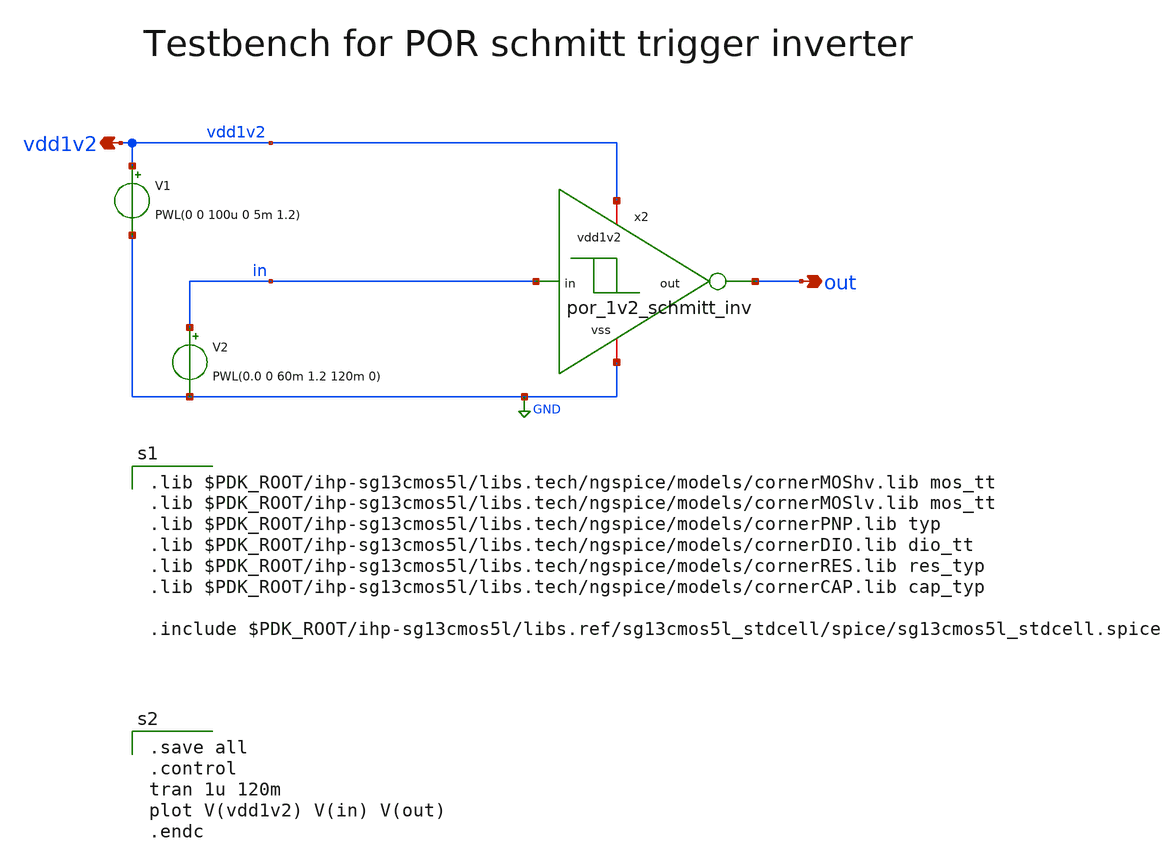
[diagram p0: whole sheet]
** sch_path: xschem/schmitt_tb.sch
**.subckt schmitt_tb vdd1v2 out
*.opin vdd1v2
*.opin out
V1 vdd1v2 GND PWL(0 0 100u 0 5m 1.2)
V2 in GND PWL(0.0 0 60m 1.2 120m 0)
x2 vdd1v2 in out GND por_1v2_schmitt_inv
**** begin user architecture code

.save all
.control
tran 1u 120m
plot V(vdd1v2) V(in) V(out)
.endc


.lib $PDK_ROOT/ihp-sg13cmos5l/libs.tech/ngspice/models/cornerMOShv.lib mos_tt
.lib $PDK_ROOT/ihp-sg13cmos5l/libs.tech/ngspice/models/cornerMOSlv.lib mos_tt
.lib $PDK_ROOT/ihp-sg13cmos5l/libs.tech/ngspice/models/cornerPNP.lib typ
.lib $PDK_ROOT/ihp-sg13cmos5l/libs.tech/ngspice/models/cornerDIO.lib dio_tt
.lib $PDK_ROOT/ihp-sg13cmos5l/libs.tech/ngspice/models/cornerRES.lib res_typ
.lib $PDK_ROOT/ihp-sg13cmos5l/libs.tech/ngspice/models/cornerCAP.lib cap_typ

.include $PDK_ROOT/ihp-sg13cmos5l/libs.ref/sg13cmos5l_stdcell/spice/sg13cmos5l_stdcell.spice

**** end user architecture code
**.ends

* expanding   symbol:  por_1v2_schmitt_inv.sym # of pins=4
** sym_path: xschem/por_1v2_schmitt_inv.sym
** sch_path: xschem/por_1v2_schmitt_inv.sch
.subckt por_1v2_schmitt_inv vdd1v2 in out vss
*.iopin vdd1v2
*.iopin vss
*.ipin in
*.opin out
XM7 out in n1 vss sg13_lv_nmos w=0.7u l=0.13u ng=2 m=1 mm_ok=1
XM8 p1 in vdd1v2 vdd1v2 sg13_lv_pmos w=1.4u l=0.13u ng=4 m=1 mm_ok=1
XM2 out in p1 vdd1v2 sg13_lv_pmos w=0.35u l=0.13u ng=1 m=1 mm_ok=1
XM3 vss out p1 vdd1v2 sg13_lv_pmos w=1.4u l=0.26u ng=1 m=1 mm_ok=1
XM1 n1 in vss vss sg13_lv_nmos w=0.7u l=0.13u ng=2 m=1 mm_ok=1
XM4 vdd1v2 out n1 vss sg13_lv_nmos w=2.8u l=0.26u ng=1 m=1 mm_ok=1
.ends

.GLOBAL GND
.end
